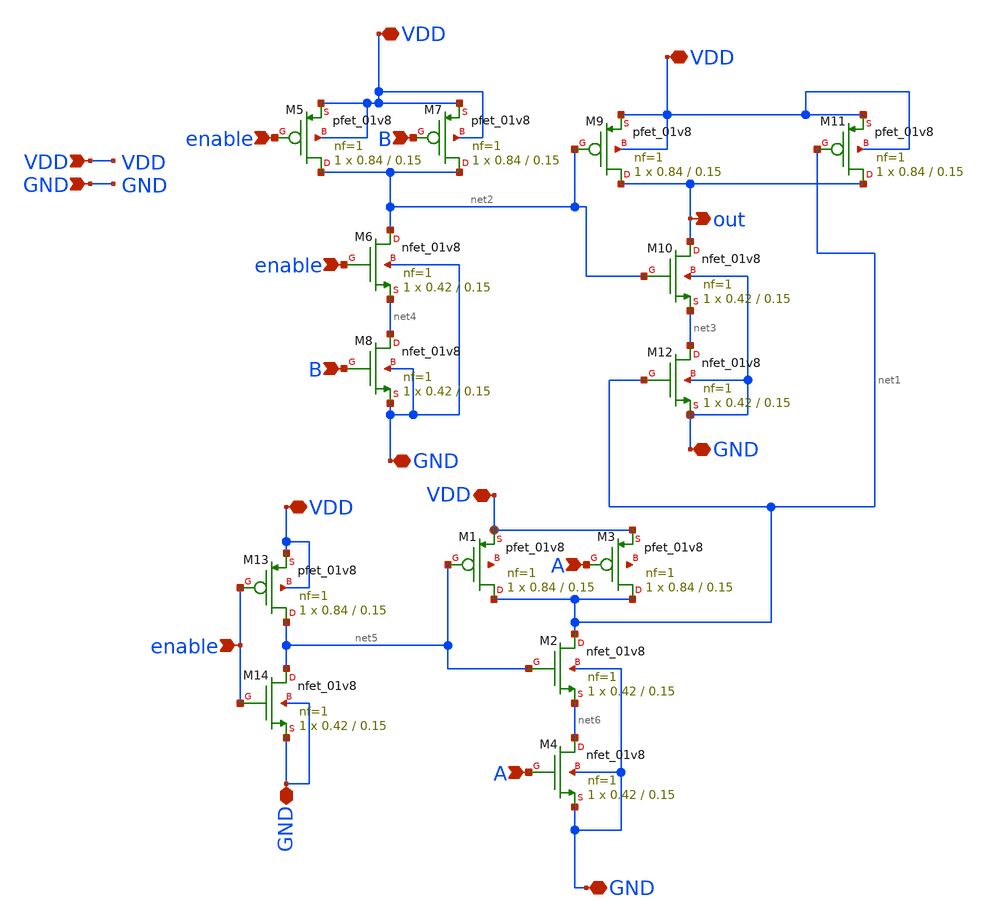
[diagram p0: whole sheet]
** sch_path: Register/xschem/mux.sch
**.subckt mux out A VDD GND VDD GND VDD VDD VDD GND GND GND enable enable B B A enable
*.opin out
*.ipin A
*.ipin VDD
*.ipin GND
*.iopin VDD
*.iopin GND
*.iopin VDD
*.iopin VDD
*.iopin VDD
*.iopin GND
*.iopin GND
*.iopin GND
*.ipin enable
*.ipin enable
*.ipin B
*.ipin B
*.ipin A
*.ipin enable
XM1 net1 net5 VDD net7 sky130_fd_pr__pfet_01v8 L=0.15 W=0.84 nf=1 ad='int((nf+1)/2) * W/nf * 0.29' as='int((nf+2)/2) * W/nf * 0.29'
+ pd='2*int((nf+1)/2) * (W/nf + 0.29)' ps='2*int((nf+2)/2) * (W/nf + 0.29)' nrd='0.29 / W' nrs='0.29 / W'
+ sa=0 sb=0 sd=0 mult=1 m=1
XM2 net1 net5 net6 GND sky130_fd_pr__nfet_01v8 L=0.15 W=0.42 nf=1 ad='int((nf+1)/2) * W/nf * 0.29' as='int((nf+2)/2) * W/nf * 0.29'
+ pd='2*int((nf+1)/2) * (W/nf + 0.29)' ps='2*int((nf+2)/2) * (W/nf + 0.29)' nrd='0.29 / W' nrs='0.29 / W'
+ sa=0 sb=0 sd=0 mult=1 m=1
XM3 net1 A VDD net8 sky130_fd_pr__pfet_01v8 L=0.15 W=0.84 nf=1 ad='int((nf+1)/2) * W/nf * 0.29' as='int((nf+2)/2) * W/nf * 0.29'
+ pd='2*int((nf+1)/2) * (W/nf + 0.29)' ps='2*int((nf+2)/2) * (W/nf + 0.29)' nrd='0.29 / W' nrs='0.29 / W'
+ sa=0 sb=0 sd=0 mult=1 m=1
XM4 net6 A GND GND sky130_fd_pr__nfet_01v8 L=0.15 W=0.42 nf=1 ad='int((nf+1)/2) * W/nf * 0.29' as='int((nf+2)/2) * W/nf * 0.29'
+ pd='2*int((nf+1)/2) * (W/nf + 0.29)' ps='2*int((nf+2)/2) * (W/nf + 0.29)' nrd='0.29 / W' nrs='0.29 / W'
+ sa=0 sb=0 sd=0 mult=1 m=1
XM5 net2 enable VDD VDD sky130_fd_pr__pfet_01v8 L=0.15 W=0.84 nf=1 ad='int((nf+1)/2) * W/nf * 0.29' as='int((nf+2)/2) * W/nf * 0.29'
+ pd='2*int((nf+1)/2) * (W/nf + 0.29)' ps='2*int((nf+2)/2) * (W/nf + 0.29)' nrd='0.29 / W' nrs='0.29 / W'
+ sa=0 sb=0 sd=0 mult=1 m=1
XM6 net2 enable net4 GND sky130_fd_pr__nfet_01v8 L=0.15 W=0.42 nf=1 ad='int((nf+1)/2) * W/nf * 0.29'
+ as='int((nf+2)/2) * W/nf * 0.29' pd='2*int((nf+1)/2) * (W/nf + 0.29)' ps='2*int((nf+2)/2) * (W/nf + 0.29)'
+ nrd='0.29 / W' nrs='0.29 / W' sa=0 sb=0 sd=0 mult=1 m=1
XM7 net2 B VDD VDD sky130_fd_pr__pfet_01v8 L=0.15 W=0.84 nf=1 ad='int((nf+1)/2) * W/nf * 0.29' as='int((nf+2)/2) * W/nf * 0.29'
+ pd='2*int((nf+1)/2) * (W/nf + 0.29)' ps='2*int((nf+2)/2) * (W/nf + 0.29)' nrd='0.29 / W' nrs='0.29 / W'
+ sa=0 sb=0 sd=0 mult=1 m=1
XM8 net4 B GND GND sky130_fd_pr__nfet_01v8 L=0.15 W=0.42 nf=1 ad='int((nf+1)/2) * W/nf * 0.29' as='int((nf+2)/2) * W/nf * 0.29'
+ pd='2*int((nf+1)/2) * (W/nf + 0.29)' ps='2*int((nf+2)/2) * (W/nf + 0.29)' nrd='0.29 / W' nrs='0.29 / W'
+ sa=0 sb=0 sd=0 mult=1 m=1
XM9 out net2 VDD VDD sky130_fd_pr__pfet_01v8 L=0.15 W=0.84 nf=1 ad='int((nf+1)/2) * W/nf * 0.29' as='int((nf+2)/2) * W/nf * 0.29'
+ pd='2*int((nf+1)/2) * (W/nf + 0.29)' ps='2*int((nf+2)/2) * (W/nf + 0.29)' nrd='0.29 / W' nrs='0.29 / W'
+ sa=0 sb=0 sd=0 mult=1 m=1
XM10 out net2 net3 GND sky130_fd_pr__nfet_01v8 L=0.15 W=0.42 nf=1 ad='int((nf+1)/2) * W/nf * 0.29' as='int((nf+2)/2) * W/nf * 0.29'
+ pd='2*int((nf+1)/2) * (W/nf + 0.29)' ps='2*int((nf+2)/2) * (W/nf + 0.29)' nrd='0.29 / W' nrs='0.29 / W'
+ sa=0 sb=0 sd=0 mult=1 m=1
XM11 out net1 VDD VDD sky130_fd_pr__pfet_01v8 L=0.15 W=0.84 nf=1 ad='int((nf+1)/2) * W/nf * 0.29' as='int((nf+2)/2) * W/nf * 0.29'
+ pd='2*int((nf+1)/2) * (W/nf + 0.29)' ps='2*int((nf+2)/2) * (W/nf + 0.29)' nrd='0.29 / W' nrs='0.29 / W'
+ sa=0 sb=0 sd=0 mult=1 m=1
XM12 net3 net1 GND GND sky130_fd_pr__nfet_01v8 L=0.15 W=0.42 nf=1 ad='int((nf+1)/2) * W/nf * 0.29' as='int((nf+2)/2) * W/nf * 0.29'
+ pd='2*int((nf+1)/2) * (W/nf + 0.29)' ps='2*int((nf+2)/2) * (W/nf + 0.29)' nrd='0.29 / W' nrs='0.29 / W'
+ sa=0 sb=0 sd=0 mult=1 m=1
XM13 net5 enable VDD VDD sky130_fd_pr__pfet_01v8 L=0.15 W=0.84 nf=1 ad='int((nf+1)/2) * W/nf * 0.29'
+ as='int((nf+2)/2) * W/nf * 0.29' pd='2*int((nf+1)/2) * (W/nf + 0.29)' ps='2*int((nf+2)/2) * (W/nf + 0.29)'
+ nrd='0.29 / W' nrs='0.29 / W' sa=0 sb=0 sd=0 mult=1 m=1
XM14 net5 enable GND GND sky130_fd_pr__nfet_01v8 L=0.15 W=0.42 nf=1 ad='int((nf+1)/2) * W/nf * 0.29'
+ as='int((nf+2)/2) * W/nf * 0.29' pd='2*int((nf+1)/2) * (W/nf + 0.29)' ps='2*int((nf+2)/2) * (W/nf + 0.29)'
+ nrd='0.29 / W' nrs='0.29 / W' sa=0 sb=0 sd=0 mult=1 m=1
**.ends
.end
